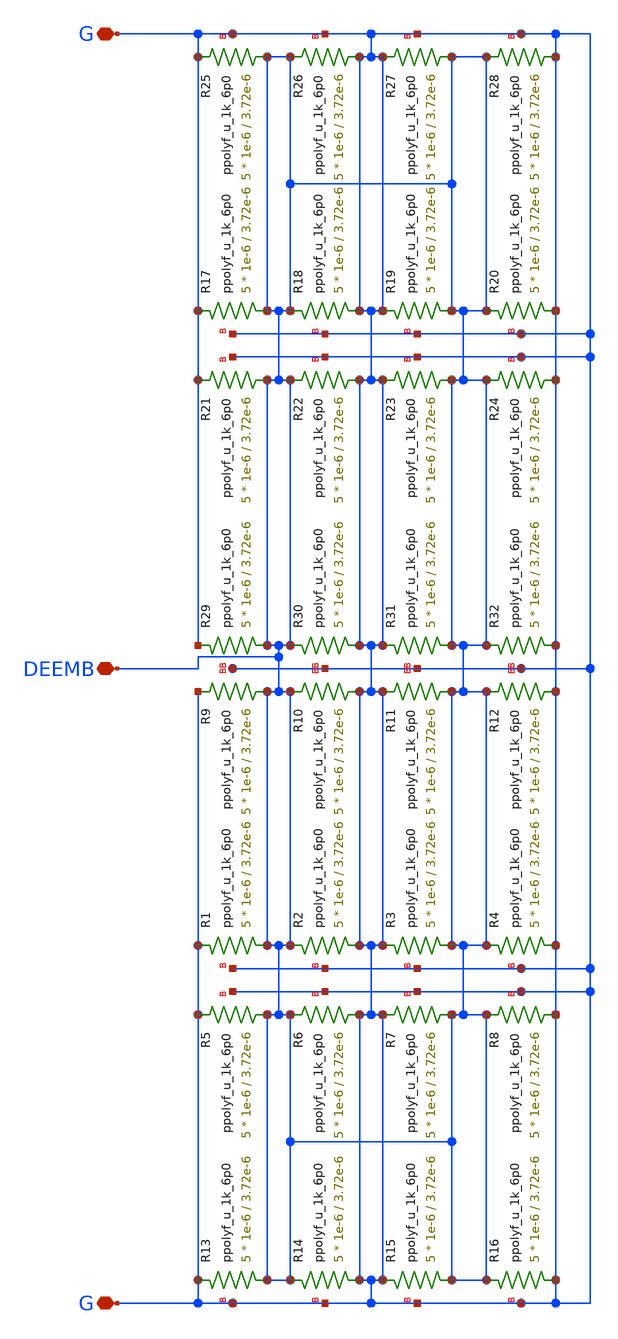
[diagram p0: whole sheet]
** sch_path: xschem/DEEMB_0P5R.sch
**.subckt DEEMB_0P5R G DEEMB G
*.iopin G
*.iopin DEEMB
*.iopin G
XR1 DEEMB G G ppolyf_u_1k_6p0 r_width=1e-6 r_length=3.72e-6 m=5
XR2 G DEEMB G ppolyf_u_1k_6p0 r_width=1e-6 r_length=3.72e-6 m=5
XR3 DEEMB G G ppolyf_u_1k_6p0 r_width=1e-6 r_length=3.72e-6 m=5
XR4 G DEEMB G ppolyf_u_1k_6p0 r_width=1e-6 r_length=3.72e-6 m=5
XR5 DEEMB G G ppolyf_u_1k_6p0 r_width=1e-6 r_length=3.72e-6 m=5
XR6 G DEEMB G ppolyf_u_1k_6p0 r_width=1e-6 r_length=3.72e-6 m=5
XR7 DEEMB G G ppolyf_u_1k_6p0 r_width=1e-6 r_length=3.72e-6 m=5
XR8 G DEEMB G ppolyf_u_1k_6p0 r_width=1e-6 r_length=3.72e-6 m=5
XR9 DEEMB G G ppolyf_u_1k_6p0 r_width=1e-6 r_length=3.72e-6 m=5
XR10 G DEEMB G ppolyf_u_1k_6p0 r_width=1e-6 r_length=3.72e-6 m=5
XR11 DEEMB G G ppolyf_u_1k_6p0 r_width=1e-6 r_length=3.72e-6 m=5
XR12 G DEEMB G ppolyf_u_1k_6p0 r_width=1e-6 r_length=3.72e-6 m=5
XR13 DEEMB G G ppolyf_u_1k_6p0 r_width=1e-6 r_length=3.72e-6 m=5
XR14 G DEEMB G ppolyf_u_1k_6p0 r_width=1e-6 r_length=3.72e-6 m=5
XR15 DEEMB G G ppolyf_u_1k_6p0 r_width=1e-6 r_length=3.72e-6 m=5
XR16 G DEEMB G ppolyf_u_1k_6p0 r_width=1e-6 r_length=3.72e-6 m=5
XR17 DEEMB G G ppolyf_u_1k_6p0 r_width=1e-6 r_length=3.72e-6 m=5
XR18 G DEEMB G ppolyf_u_1k_6p0 r_width=1e-6 r_length=3.72e-6 m=5
XR19 DEEMB G G ppolyf_u_1k_6p0 r_width=1e-6 r_length=3.72e-6 m=5
XR20 G DEEMB G ppolyf_u_1k_6p0 r_width=1e-6 r_length=3.72e-6 m=5
XR21 DEEMB G G ppolyf_u_1k_6p0 r_width=1e-6 r_length=3.72e-6 m=5
XR22 G DEEMB G ppolyf_u_1k_6p0 r_width=1e-6 r_length=3.72e-6 m=5
XR23 DEEMB G G ppolyf_u_1k_6p0 r_width=1e-6 r_length=3.72e-6 m=5
XR24 G DEEMB G ppolyf_u_1k_6p0 r_width=1e-6 r_length=3.72e-6 m=5
XR25 DEEMB G G ppolyf_u_1k_6p0 r_width=1e-6 r_length=3.72e-6 m=5
XR26 G DEEMB G ppolyf_u_1k_6p0 r_width=1e-6 r_length=3.72e-6 m=5
XR27 DEEMB G G ppolyf_u_1k_6p0 r_width=1e-6 r_length=3.72e-6 m=5
XR28 G DEEMB G ppolyf_u_1k_6p0 r_width=1e-6 r_length=3.72e-6 m=5
XR29 DEEMB G G ppolyf_u_1k_6p0 r_width=1e-6 r_length=3.72e-6 m=5
XR30 G DEEMB G ppolyf_u_1k_6p0 r_width=1e-6 r_length=3.72e-6 m=5
XR31 DEEMB G G ppolyf_u_1k_6p0 r_width=1e-6 r_length=3.72e-6 m=5
XR32 G DEEMB G ppolyf_u_1k_6p0 r_width=1e-6 r_length=3.72e-6 m=5
**.ends
.end
